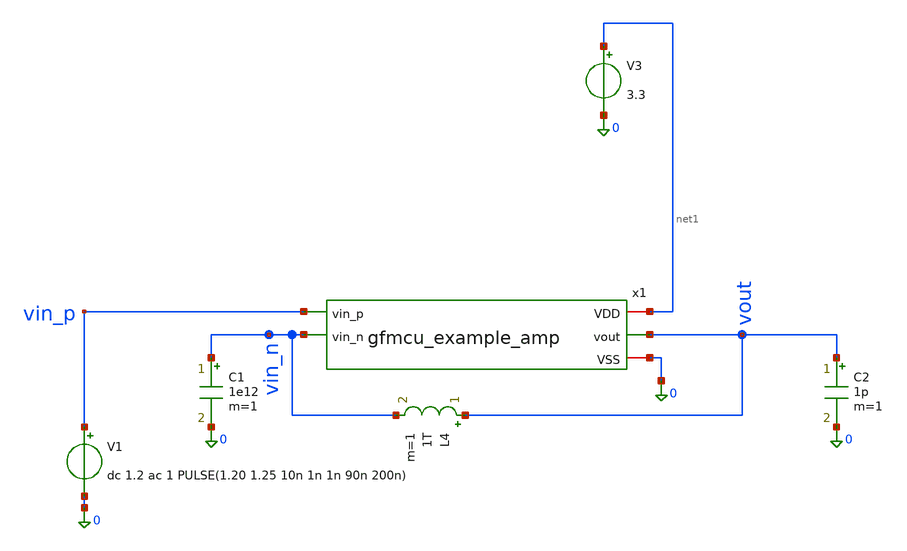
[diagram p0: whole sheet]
** sch_path: xschem/tb_example_amp.sch
**.subckt tb_example_amp
V3 net1 0 3.3
C2 vout 0 1p m=1
V1 vin_p 0 dc 1.2 ac 1 PULSE(1.20 1.25 10n 1n 1n 90n 200n)
L4 vout vin_n 1T m=1
C1 vin_n 0 1e12 m=1
x1 net1 vin_n vin_p vout 0 gfmcu_example_amp
**** begin user architecture code


* GF180MCU Global Process & Noise Parameters (Must be before .lib)
.param fnoicor = 0
.param sw_stat_global = 0
.param sw_stat_mismatch = 1

* PDK Model Include (MOSFETs)
.include /foss/pdks/ciel/gf180mcu/versions/026824c7969ce6f4fc9678e6ca04b0a06a596c4b/gf180mcuD/libs.tech/ngspice/design.ngspice
.lib /foss/pdks/ciel/gf180mcu/versions/026824c7969ce6f4fc9678e6ca04b0a06a596c4b/gf180mcuD/libs.tech/ngspice/sm141064.ngspice typical
.lib /foss/pdks/ciel/gf180mcu/versions/026824c7969ce6f4fc9678e6ca04b0a06a596c4b/gf180mcuD/libs.tech/ngspice/sm141064.ngspice res_typical

* MIM Capacitor Model (bypasses missing OSDI library)
.subckt cap_mim_2f0ff c0 c1 c_width=1e-6 c_length=1e-6
C_mim c0 c1 2.5p
.ends cap_mim_2f0ff

* Remove any .ac or .tran lines outside .control so they don't run prematurely
.save all

.control
* ======================================================================
* 1. DC OPERATING POINT & TRANSISTOR SATURATION CHECK
* ======================================================================
op

let v_inp_dc   = v(vin_p)
let v_inn_dc   = v(vin_n)
let v_out_dc   = v(vout)
let i_vdd_ua   = abs(v3#branch) * 1e6
let p_total_mw = i_vdd_ua * 3.3 / 1e3

echo ======================================================================
echo                   1. DC OPERATING VOLTAGES & POWER
echo ======================================================================
print v_inp_dc v_inn_dc v_out_dc
print i_vdd_ua p_total_mw

echo =========================================================
echo             2. TRANSISTOR SATURATION CHECK
echo =========================================================
echo   If Margin is POSITIVE (+) -> SATURATION (GOOD)
echo   If Margin is NEGATIVE (-) -> TRIODE/LINEAR (BAD - KILLS GAIN)
echo =========================================================

* NMOS Tail (XM3 in stg1)
let vds_tail   = abs(@m.x1.xm3.m0[vds])
let vdsat_tail = abs(@m.x1.xm3.m0[vdsat])
let marg_tail  = vds_tail - vdsat_tail

* NMOS Input (XM1 in stg1)
let vds_in     = abs(@m.x1.xm1.m0[vds])
let vdsat_in   = abs(@m.x1.xm1.m0[vdsat])
let marg_in    = vds_in - vdsat_in

* NMOS Cascode (XM4 in stg1)
let vds_casc   = abs(@m.x1.xm4.m0[vds])
let vdsat_casc = abs(@m.x1.xm4.m0[vdsat])
let marg_casc  = vds_casc - vdsat_casc

* PMOS Cascode (XM8 in stg1)
let vds_pcasc   = abs(@m.x1.xm8.m0[vds])
let vdsat_pcasc = abs(@m.x1.xm8.m0[vdsat])
let marg_pcasc  = vds_pcasc - vdsat_pcasc

* PMOS Mirror (XM10 in stg1)
let vds_pmir   = abs(@m.x1.xm10.m0[vds])
let vdsat_pmir = abs(@m.x1.xm10.m0[vdsat])
let marg_pmir  = vds_pmir - vdsat_pmir

echo --- NMOS Tail (XM3) ---
print vds_tail vdsat_tail marg_tail
echo --- NMOS Input (XM1) ---
print vds_in vdsat_in marg_in
echo --- NMOS Cascode (XM4) ---
print vds_casc vdsat_casc marg_casc
echo --- PMOS Cascode (XM8) ---
print vds_pcasc vdsat_pcasc marg_pcasc
echo --- PMOS Mirror (XM10) ---
print vds_pmir vdsat_pmir marg_pmir
echo ======================================================================

* ======================================================================
* 3. AC FREQUENCY RESPONSE (OPEN-LOOP: L4=1e12, C1=1e12)
* ======================================================================
alter l4 = 1e12
alter c1 = 1e12
ac dec 35 1 5G

let v_out_ac  = v(vout)
let gain_db   = db(v_out_ac)
let phase_deg = cph(v_out_ac) * 180 / 3.1415926535

meas ac dc_gain find gain_db at=1
let g_3db = dc_gain - 3
meas ac f_3db when gain_db = g_3db
meas ac f_ugbw when gain_db = 0
meas ac ph_ugbw find phase_deg when gain_db = 0
let pm = 180 + ph_ugbw

echo ======================================================================
echo                   3. AC FREQUENCY RESPONSE RESULTS
echo ======================================================================
print dc_gain
print f_3db
print f_ugbw
print pm
echo ======================================================================

* ======================================================================
* 4. TRANSIENT & SLEW RATE (CLOSED-LOOP UNITY-GAIN: L4=1p, C1=1f)
* ======================================================================
alter l4 = 1e-12
alter c1 = 1e-18
tran 0.1n 1000n

meas tran v_init find v(vout) at=9n
meas tran v_max MAX v(vout) from=10n to=100n
meas tran v_min MIN v(vout) from=100n to=200n

* 20% to 80% levels (1.21V to 1.24V) with from=10n to ignore startup settling
meas tran t_rise TRIG v(vout) VAL=1.21 RISE=1 TARG v(vout) VAL=1.24 RISE=1 from=10n
meas tran t_fall TRIG v(vout) VAL=1.24 FALL=1 TARG v(vout) VAL=1.21 FALL=1 from=50n

* Calculate Slew Rates
let sr_rise_v_us = (0.03 / t_rise) / 1e6
let sr_fall_v_us = (0.03 / t_fall) / 1e6

echo ======================================================================
echo                   4. TRANSIENT & SLEW RATE RESULTS
echo ======================================================================
print v_init v_max v_min
print t_rise sr_rise_v_us
print t_fall sr_fall_v_us
echo ======================================================================

* ======================================================================
* 5. PLOTS
* ======================================================================
setplot ac1
plot db(v(vout)) title 'Open-Loop Gain (dB)'
plot (cph(v(vout))*180/3.14159265) title 'Open-Loop Phase (Deg)'

setplot tran1
plot v(vout) v(vin_p) title 'Closed-Loop Transient Step Response'
.endc


**** end user architecture code
**.ends

* expanding   symbol:  ttgf-ece298-analog-op-amp/xschem/gfmcu_example_amp.sym # of pins=5
** sym_path: xschem/gfmcu_example_amp.sym
** sch_path: xschem/gfmcu_example_amp.sch
.subckt gfmcu_example_amp VDD vin_n vin_p vout VSS
*.ipin vin_n
*.ipin vin_p
*.opin vout
*.iopin VSS
*.iopin VDD
XR1 net1 VDD VDD ppolyf_u r_width=0.5 r_length=40 m=1
XM1 net6 net2 net1 VDD pfet_03v3 L=0.84u W=4u nf=4 ad='int((nf+1)/2) * W/nf * 0.18u' as='int((nf+2)/2)
+ * W/nf * 0.18u' pd='2*int((nf+1)/2) * (W/nf + 0.18u)' ps='2*int((nf+2)/2) * (W/nf + 0.18u)' nrd='0.18u
+ / W' nrs='0.18u / W' sa=0 sb=0 sd=0 m=2 par=2
XM2 net3 net3 VDD VDD pfet_03v3 L=0.28u W=4u nf=4 ad='int((nf+1)/2) * W/nf * 0.18u' as='int((nf+2)/2)
+ * W/nf * 0.18u' pd='2*int((nf+1)/2) * (W/nf + 0.18u)' ps='2*int((nf+2)/2) * (W/nf + 0.18u)' nrd='0.18u
+ / W' nrs='0.18u / W' sa=0 sb=0 sd=0 m=2 par=2
XM3 net2 net2 net3 VDD pfet_03v3 L=0.84u W=4u nf=4 ad='int((nf+1)/2) * W/nf * 0.18u' as='int((nf+2)/2)
+ * W/nf * 0.18u' pd='2*int((nf+1)/2) * (W/nf + 0.18u)' ps='2*int((nf+2)/2) * (W/nf + 0.18u)' nrd='0.18u
+ / W' nrs='0.18u / W' sa=0 sb=0 sd=0 m=2 par=2
XM4 net6 net6 net5 VSS nfet_03v3 L=0.84u W=4u nf=4 ad='int((nf+1)/2) * W/nf * 0.18u' as='int((nf+2)/2)
+ * W/nf * 0.18u' pd='2*int((nf+1)/2) * (W/nf + 0.18u)' ps='2*int((nf+2)/2) * (W/nf + 0.18u)' nrd='0.18u
+ / W' nrs='0.18u / W' sa=0 sb=0 sd=0 m=2 par=2
XM5 net5 net5 VSS VSS nfet_03v3 L=0.84u W=4u nf=4 ad='int((nf+1)/2) * W/nf * 0.18u' as='int((nf+2)/2)
+ * W/nf * 0.18u' pd='2*int((nf+1)/2) * (W/nf + 0.18u)' ps='2*int((nf+2)/2) * (W/nf + 0.18u)' nrd='0.18u
+ / W' nrs='0.18u / W' sa=0 sb=0 sd=0 m=2 par=2
XM6 net2 net6 net4 VSS nfet_03v3 L=0.84u W=4u nf=4 ad='int((nf+1)/2) * W/nf * 0.18u' as='int((nf+2)/2)
+ * W/nf * 0.18u' pd='2*int((nf+1)/2) * (W/nf + 0.18u)' ps='2*int((nf+2)/2) * (W/nf + 0.18u)' nrd='0.18u
+ / W' nrs='0.18u / W' sa=0 sb=0 sd=0 m=2 par=2
XM7 net4 net5 VSS VSS nfet_03v3 L=0.84u W=4u nf=4 ad='int((nf+1)/2) * W/nf * 0.18u' as='int((nf+2)/2)
+ * W/nf * 0.18u' pd='2*int((nf+1)/2) * (W/nf + 0.18u)' ps='2*int((nf+2)/2) * (W/nf + 0.18u)' nrd='0.18u
+ / W' nrs='0.18u / W' sa=0 sb=0 sd=0 m=2 par=2
XM8 net7 net5 VSS VSS nfet_03v3 L=0.84u W=4u nf=4 ad='int((nf+1)/2) * W/nf * 0.18u' as='int((nf+2)/2)
+ * W/nf * 0.18u' pd='2*int((nf+1)/2) * (W/nf + 0.18u)' ps='2*int((nf+2)/2) * (W/nf + 0.18u)' nrd='0.18u
+ / W' nrs='0.18u / W' sa=0 sb=0 sd=0 m=2 par=2
XM9 net7 net7 VDD VDD pfet_03v3 L=0.84u W=4u nf=4 ad='int((nf+1)/2) * W/nf * 0.18u' as='int((nf+2)/2)
+ * W/nf * 0.18u' pd='2*int((nf+1)/2) * (W/nf + 0.18u)' ps='2*int((nf+2)/2) * (W/nf + 0.18u)' nrd='0.18u
+ / W' nrs='0.18u / W' sa=0 sb=0 sd=0 m=2 par=2
XM10 net8 net9 VDD VDD pfet_03v3 L=0.84u W=4u nf=4 ad='int((nf+1)/2) * W/nf * 0.18u' as='int((nf+2)/2)
+ * W/nf * 0.18u' pd='2*int((nf+1)/2) * (W/nf + 0.18u)' ps='2*int((nf+2)/2) * (W/nf + 0.18u)' nrd='0.18u
+ / W' nrs='0.18u / W' sa=0 sb=0 sd=0 m=2 par=2
XM12 net11 vin_p net8 VDD pfet_03v3 L=0.84u W=4u nf=4 ad='int((nf+1)/2) * W/nf * 0.18u' as='int((nf+2)/2)
+ * W/nf * 0.18u' pd='2*int((nf+1)/2) * (W/nf + 0.18u)' ps='2*int((nf+2)/2) * (W/nf + 0.18u)' nrd='0.18u
+ / W' nrs='0.18u / W' sa=0 sb=0 sd=0 m=16 par=16
XM13 net10 vin_n net8 VDD pfet_03v3 L=0.84u W=4u nf=4 ad='int((nf+1)/2) * W/nf * 0.18u' as='int((nf+2)/2)
+ * W/nf * 0.18u' pd='2*int((nf+1)/2) * (W/nf + 0.18u)' ps='2*int((nf+2)/2) * (W/nf + 0.18u)' nrd='0.18u
+ / W' nrs='0.18u / W' sa=0 sb=0 sd=0 m=16 par=16
XM14 net12 net9 VDD VDD pfet_03v3 L=0.84u W=4u nf=4 ad='int((nf+1)/2) * W/nf * 0.18u' as='int((nf+2)/2)
+ * W/nf * 0.18u' pd='2*int((nf+1)/2) * (W/nf + 0.18u)' ps='2*int((nf+2)/2) * (W/nf + 0.18u)' nrd='0.18u
+ / W' nrs='0.18u / W' sa=0 sb=0 sd=0 m=2 par=2
XM15 net9 net13 net12 VDD pfet_03v3 L=0.84u W=4u nf=4 ad='int((nf+1)/2) * W/nf * 0.18u' as='int((nf+2)/2)
+ * W/nf * 0.18u' pd='2*int((nf+1)/2) * (W/nf + 0.18u)' ps='2*int((nf+2)/2) * (W/nf + 0.18u)' nrd='0.18u
+ / W' nrs='0.18u / W' sa=0 sb=0 sd=0 m=2 par=2
XR2 net13 net9 VDD ppolyf_u r_width=0.5 r_length=20 m=1
XM16 net14 net9 VDD VDD pfet_03v3 L=0.84u W=4u nf=4 ad='int((nf+1)/2) * W/nf * 0.18u' as='int((nf+2)/2)
+ * W/nf * 0.18u' pd='2*int((nf+1)/2) * (W/nf + 0.18u)' ps='2*int((nf+2)/2) * (W/nf + 0.18u)' nrd='0.18u
+ / W' nrs='0.18u / W' sa=0 sb=0 sd=0 m=2 par=2
XM18 vout net13 net14 VDD pfet_03v3 L=0.84u W=4u nf=4 ad='int((nf+1)/2) * W/nf * 0.18u' as='int((nf+2)/2)
+ * W/nf * 0.18u' pd='2*int((nf+1)/2) * (W/nf + 0.18u)' ps='2*int((nf+2)/2) * (W/nf + 0.18u)' nrd='0.18u
+ / W' nrs='0.18u / W' sa=0 sb=0 sd=0 m=2 par=2
XM19 net13 net6 net11 VSS nfet_03v3 L=0.84u W=4u nf=4 ad='int((nf+1)/2) * W/nf * 0.18u' as='int((nf+2)/2)
+ * W/nf * 0.18u' pd='2*int((nf+1)/2) * (W/nf + 0.18u)' ps='2*int((nf+2)/2) * (W/nf + 0.18u)' nrd='0.18u
+ / W' nrs='0.18u / W' sa=0 sb=0 sd=0 m=2 par=2
XM20 net11 net5 VSS VSS nfet_03v3 L=0.84u W=4u nf=4 ad='int((nf+1)/2) * W/nf * 0.18u' as='int((nf+2)/2)
+ * W/nf * 0.18u' pd='2*int((nf+1)/2) * (W/nf + 0.18u)' ps='2*int((nf+2)/2) * (W/nf + 0.18u)' nrd='0.18u
+ / W' nrs='0.18u / W' sa=0 sb=0 sd=0 m=2 par=2
XM21 vout net6 net10 VSS nfet_03v3 L=0.84u W=4u nf=4 ad='int((nf+1)/2) * W/nf * 0.18u' as='int((nf+2)/2)
+ * W/nf * 0.18u' pd='2*int((nf+1)/2) * (W/nf + 0.18u)' ps='2*int((nf+2)/2) * (W/nf + 0.18u)' nrd='0.18u
+ / W' nrs='0.18u / W' sa=0 sb=0 sd=0 m=2 par=2
XM22 net10 net5 VSS VSS nfet_03v3 L=0.84u W=4u nf=4 ad='int((nf+1)/2) * W/nf * 0.18u' as='int((nf+2)/2)
+ * W/nf * 0.18u' pd='2*int((nf+1)/2) * (W/nf + 0.18u)' ps='2*int((nf+2)/2) * (W/nf + 0.18u)' nrd='0.18u
+ / W' nrs='0.18u / W' sa=0 sb=0 sd=0 m=2 par=2
.ends

.end
